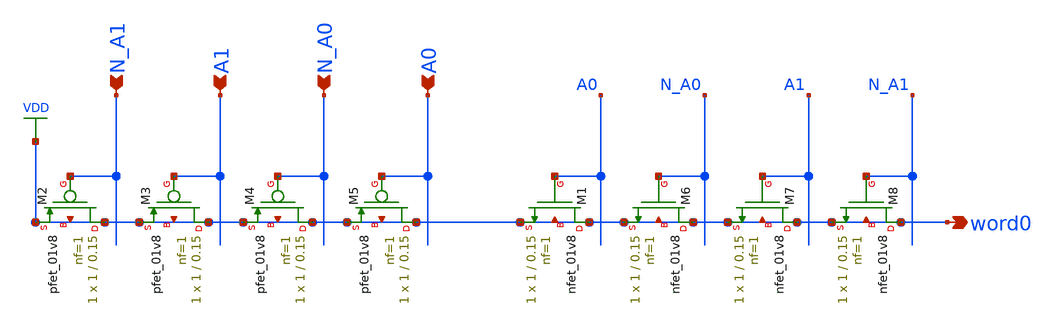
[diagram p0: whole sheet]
** sch_path: circuits/xschem/partials/decoder_row.sch
**.subckt decoder_row N_A1 A1 N_A0 A0 word0
*.ipin N_A1
*.ipin A1
*.ipin N_A0
*.ipin A0
*.opin word0
XM1 VDD A0 VDD VDD sky130_fd_pr__nfet_01v8 L=0.15 W=1 nf=1 ad='int((nf+1)/2) * W/nf * 0.29' as='int((nf+2)/2) * W/nf * 0.29'
+ pd='2*int((nf+1)/2) * (W/nf + 0.29)' ps='2*int((nf+2)/2) * (W/nf + 0.29)' nrd='0.29 / W' nrs='0.29 / W'
+ sa=0 sb=0 sd=0 mult=1 m=1
XM2 VDD N_A1 VDD VDD sky130_fd_pr__pfet_01v8 L=0.15 W=1 nf=1 ad='int((nf+1)/2) * W/nf * 0.29' as='int((nf+2)/2) * W/nf * 0.29'
+ pd='2*int((nf+1)/2) * (W/nf + 0.29)' ps='2*int((nf+2)/2) * (W/nf + 0.29)' nrd='0.29 / W' nrs='0.29 / W'
+ sa=0 sb=0 sd=0 mult=1 m=1
XM3 VDD A1 VDD VDD sky130_fd_pr__pfet_01v8 L=0.15 W=1 nf=1 ad='int((nf+1)/2) * W/nf * 0.29' as='int((nf+2)/2) * W/nf * 0.29'
+ pd='2*int((nf+1)/2) * (W/nf + 0.29)' ps='2*int((nf+2)/2) * (W/nf + 0.29)' nrd='0.29 / W' nrs='0.29 / W'
+ sa=0 sb=0 sd=0 mult=1 m=1
XM4 VDD N_A0 VDD VDD sky130_fd_pr__pfet_01v8 L=0.15 W=1 nf=1 ad='int((nf+1)/2) * W/nf * 0.29' as='int((nf+2)/2) * W/nf * 0.29'
+ pd='2*int((nf+1)/2) * (W/nf + 0.29)' ps='2*int((nf+2)/2) * (W/nf + 0.29)' nrd='0.29 / W' nrs='0.29 / W'
+ sa=0 sb=0 sd=0 mult=1 m=1
XM5 VDD A0 VDD VDD sky130_fd_pr__pfet_01v8 L=0.15 W=1 nf=1 ad='int((nf+1)/2) * W/nf * 0.29' as='int((nf+2)/2) * W/nf * 0.29'
+ pd='2*int((nf+1)/2) * (W/nf + 0.29)' ps='2*int((nf+2)/2) * (W/nf + 0.29)' nrd='0.29 / W' nrs='0.29 / W'
+ sa=0 sb=0 sd=0 mult=1 m=1
XM6 VDD N_A0 VDD VDD sky130_fd_pr__nfet_01v8 L=0.15 W=1 nf=1 ad='int((nf+1)/2) * W/nf * 0.29' as='int((nf+2)/2) * W/nf * 0.29'
+ pd='2*int((nf+1)/2) * (W/nf + 0.29)' ps='2*int((nf+2)/2) * (W/nf + 0.29)' nrd='0.29 / W' nrs='0.29 / W'
+ sa=0 sb=0 sd=0 mult=1 m=1
XM7 VDD A1 VDD VDD sky130_fd_pr__nfet_01v8 L=0.15 W=1 nf=1 ad='int((nf+1)/2) * W/nf * 0.29' as='int((nf+2)/2) * W/nf * 0.29'
+ pd='2*int((nf+1)/2) * (W/nf + 0.29)' ps='2*int((nf+2)/2) * (W/nf + 0.29)' nrd='0.29 / W' nrs='0.29 / W'
+ sa=0 sb=0 sd=0 mult=1 m=1
XM8 VDD N_A1 VDD VDD sky130_fd_pr__nfet_01v8 L=0.15 W=1 nf=1 ad='int((nf+1)/2) * W/nf * 0.29' as='int((nf+2)/2) * W/nf * 0.29'
+ pd='2*int((nf+1)/2) * (W/nf + 0.29)' ps='2*int((nf+2)/2) * (W/nf + 0.29)' nrd='0.29 / W' nrs='0.29 / W'
+ sa=0 sb=0 sd=0 mult=1 m=1
**.ends
.GLOBAL VDD
.end
